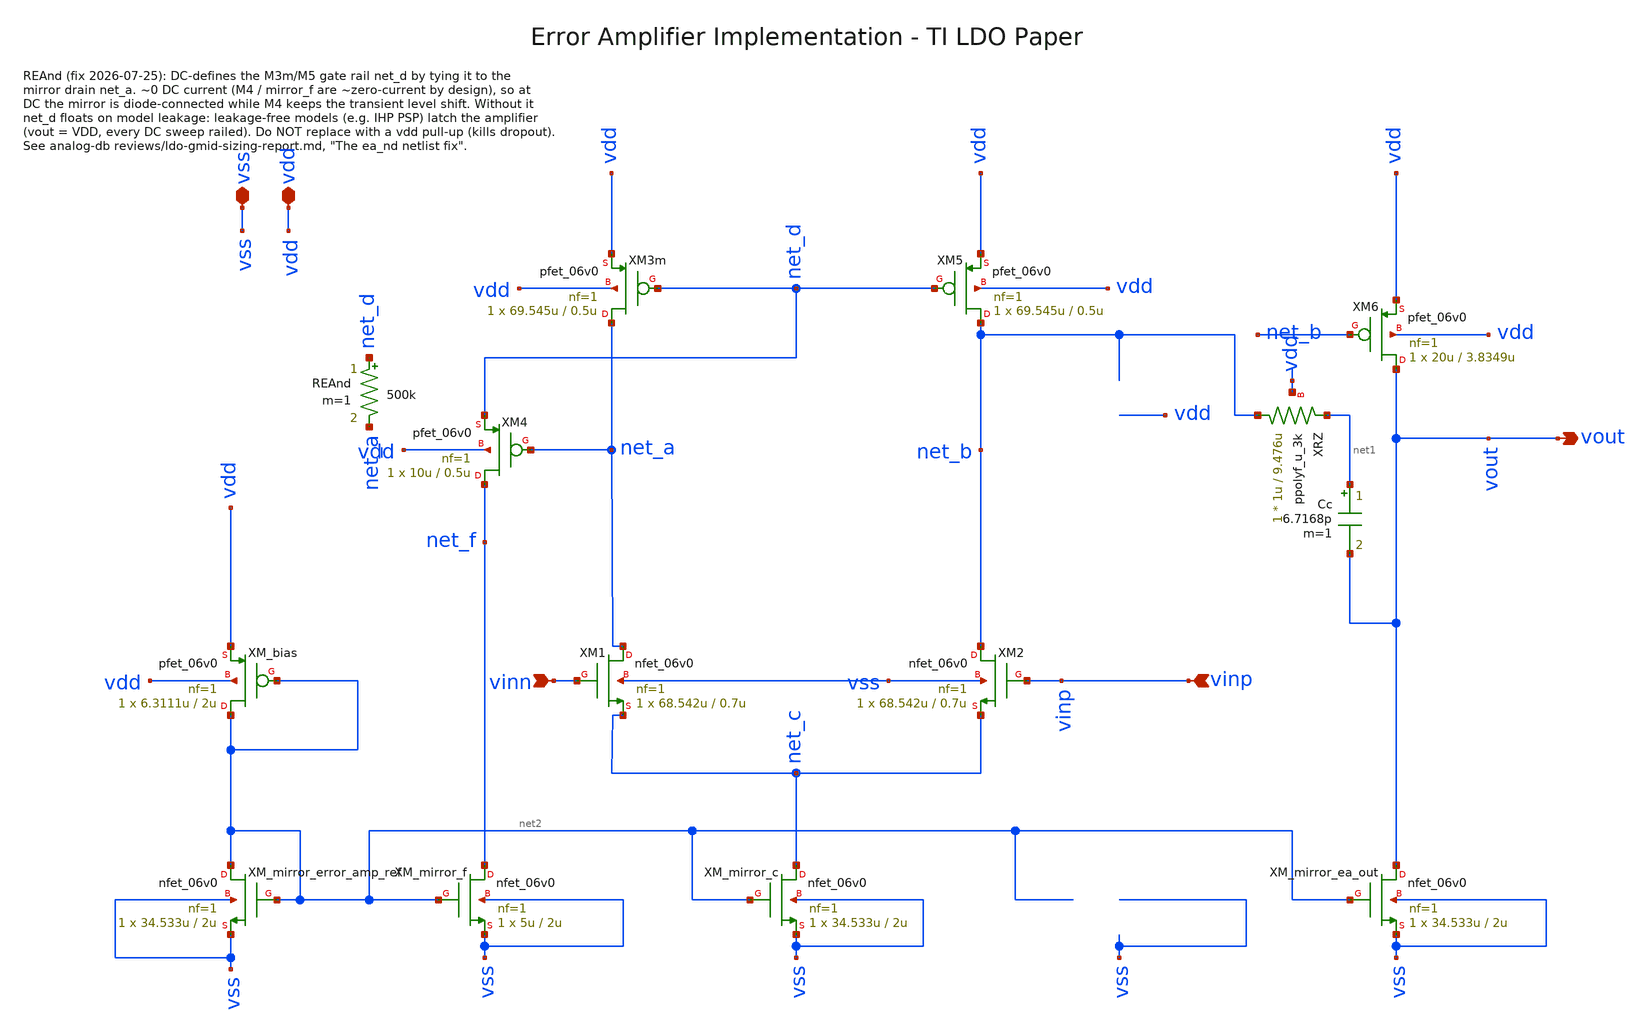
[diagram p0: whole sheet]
** sch_path: analog-db/drawings/ldo-005-ti-ldo-buffer-ref/gf180/error_amp/error_amp.sch
**.subckt error_amp vdd vss vinp vout vinn
*.iopin vdd
*.iopin vss
*.ipin vinp
*.opin vout
*.ipin vinn
XM2 net_b vinp net_c vss nfet_06v0 L=0.7u W=68.542u nf=1 ad='int((nf+1)/2) * W/nf * 0.18u' as='int((nf+2)/2) * W/nf * 0.18u'
+ pd='2*int((nf+1)/2) * (W/nf + 0.18u)' ps='2*int((nf+2)/2) * (W/nf + 0.18u)' nrd='0.18u / W' nrs='0.18u / W'
+ sa=0 sb=0 sd=0 m=1
XM3m net_a net_d vdd vdd pfet_06v0 L=0.5u W=69.545u nf=1 ad='int((nf+1)/2) * W/nf * 0.18u' as='int((nf+2)/2) * W/nf * 0.18u'
+ pd='2*int((nf+1)/2) * (W/nf + 0.18u)' ps='2*int((nf+2)/2) * (W/nf + 0.18u)' nrd='0.18u / W' nrs='0.18u / W'
+ sa=0 sb=0 sd=0 m=1
XM4 net_f net_a net_d vdd pfet_06v0 L=0.5u W=10u nf=1 ad='int((nf+1)/2) * W/nf * 0.18u' as='int((nf+2)/2) * W/nf * 0.18u'
+ pd='2*int((nf+1)/2) * (W/nf + 0.18u)' ps='2*int((nf+2)/2) * (W/nf + 0.18u)' nrd='0.18u / W' nrs='0.18u / W'
+ sa=0 sb=0 sd=0 m=1
XM5 net_b net_d vdd vdd pfet_06v0 L=0.5u W=69.545u nf=1 ad='int((nf+1)/2) * W/nf * 0.18u' as='int((nf+2)/2) * W/nf * 0.18u'
+ pd='2*int((nf+1)/2) * (W/nf + 0.18u)' ps='2*int((nf+2)/2) * (W/nf + 0.18u)' nrd='0.18u / W' nrs='0.18u / W'
+ sa=0 sb=0 sd=0 m=1
XM6 vout net_b vdd vdd pfet_06v0 L=3.8349u W=20u nf=1 ad='int((nf+1)/2) * W/nf * 0.18u' as='int((nf+2)/2) * W/nf * 0.18u'
+ pd='2*int((nf+1)/2) * (W/nf + 0.18u)' ps='2*int((nf+2)/2) * (W/nf + 0.18u)' nrd='0.18u / W' nrs='0.18u / W'
+ sa=0 sb=0 sd=0 m=1
Cc net1 vout 6.7168p m=1
XRZ net_b net1 vdd ppolyf_u_3k r_width=1u r_length=9.476u m=1
XM1 net_a vinn net_c vss nfet_06v0 L=0.7u W=68.542u nf=1 ad='int((nf+1)/2) * W/nf * 0.18u' as='int((nf+2)/2) * W/nf * 0.18u'
+ pd='2*int((nf+1)/2) * (W/nf + 0.18u)' ps='2*int((nf+2)/2) * (W/nf + 0.18u)' nrd='0.18u / W' nrs='0.18u / W'
+ sa=0 sb=0 sd=0 m=1
XM_mirror_error_amp_ref net2 net2 vss vss nfet_06v0 L=2u W=34.533u nf=1 ad='int((nf+1)/2) * W/nf * 0.18u'
+ as='int((nf+2)/2) * W/nf * 0.18u' pd='2*int((nf+1)/2) * (W/nf + 0.18u)' ps='2*int((nf+2)/2) * (W/nf + 0.18u)'
+ nrd='0.18u / W' nrs='0.18u / W' sa=0 sb=0 sd=0 m=1
XM_mirror_f net_f net2 vss vss nfet_06v0 L=2u W=5u nf=1 ad='int((nf+1)/2) * W/nf * 0.18u' as='int((nf+2)/2) * W/nf * 0.18u'
+ pd='2*int((nf+1)/2) * (W/nf + 0.18u)' ps='2*int((nf+2)/2) * (W/nf + 0.18u)' nrd='0.18u / W' nrs='0.18u / W'
+ sa=0 sb=0 sd=0 m=1
XM_mirror_c net_c net2 vss vss nfet_06v0 L=2u W=34.533u nf=1 ad='int((nf+1)/2) * W/nf * 0.18u' as='int((nf+2)/2) * W/nf * 0.18u'
+ pd='2*int((nf+1)/2) * (W/nf + 0.18u)' ps='2*int((nf+2)/2) * (W/nf + 0.18u)' nrd='0.18u / W' nrs='0.18u / W'
+ sa=0 sb=0 sd=0 m=1
XM_mirror_ea_out vout net2 vss vss nfet_06v0 L=2u W=34.533u nf=1 ad='int((nf+1)/2) * W/nf * 0.18u' as='int((nf+2)/2) * W/nf * 0.18u'
+ pd='2*int((nf+1)/2) * (W/nf + 0.18u)' ps='2*int((nf+2)/2) * (W/nf + 0.18u)' nrd='0.18u / W' nrs='0.18u / W'
+ sa=0 sb=0 sd=0 m=1
XM_bias net2 net2 vdd vdd pfet_06v0 L=2u W=6.3111u nf=1 ad='int((nf+1)/2) * W/nf * 0.18u' as='int((nf+2)/2) * W/nf * 0.18u'
+ pd='2*int((nf+1)/2) * (W/nf + 0.18u)' ps='2*int((nf+2)/2) * (W/nf + 0.18u)' nrd='0.18u / W' nrs='0.18u / W'
+ sa=0 sb=0 sd=0 m=1
REAnd net_d net_a 500k m=1
**.ends
.end
